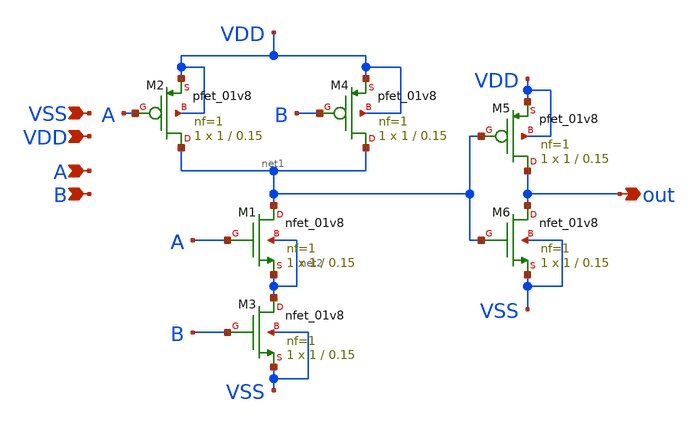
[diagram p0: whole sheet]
** sch_path: and/and2.sch
**.subckt and2 VDD A B VSS out
*.ipin VDD
*.ipin A
*.ipin B
*.ipin VSS
*.opin out
XM1 net1 A net2 net2 sky130_fd_pr__nfet_01v8 L=0.15 W=1 nf=1 ad='int((nf+1)/2) * W/nf * 0.29' as='int((nf+2)/2) * W/nf * 0.29'
+ pd='2*int((nf+1)/2) * (W/nf + 0.29)' ps='2*int((nf+2)/2) * (W/nf + 0.29)' nrd='0.29 / W' nrs='0.29 / W'
+ sa=0 sb=0 sd=0 mult=1 m=1
XM2 net1 A VDD VDD sky130_fd_pr__pfet_01v8 L=0.15 W=1 nf=1 ad='int((nf+1)/2) * W/nf * 0.29' as='int((nf+2)/2) * W/nf * 0.29'
+ pd='2*int((nf+1)/2) * (W/nf + 0.29)' ps='2*int((nf+2)/2) * (W/nf + 0.29)' nrd='0.29 / W' nrs='0.29 / W'
+ sa=0 sb=0 sd=0 mult=1 m=1
XM3 net2 B VSS VSS sky130_fd_pr__nfet_01v8 L=0.15 W=1 nf=1 ad='int((nf+1)/2) * W/nf * 0.29' as='int((nf+2)/2) * W/nf * 0.29'
+ pd='2*int((nf+1)/2) * (W/nf + 0.29)' ps='2*int((nf+2)/2) * (W/nf + 0.29)' nrd='0.29 / W' nrs='0.29 / W'
+ sa=0 sb=0 sd=0 mult=1 m=1
XM4 net1 B VDD VDD sky130_fd_pr__pfet_01v8 L=0.15 W=1 nf=1 ad='int((nf+1)/2) * W/nf * 0.29' as='int((nf+2)/2) * W/nf * 0.29'
+ pd='2*int((nf+1)/2) * (W/nf + 0.29)' ps='2*int((nf+2)/2) * (W/nf + 0.29)' nrd='0.29 / W' nrs='0.29 / W'
+ sa=0 sb=0 sd=0 mult=1 m=1
XM5 out net1 VDD VDD sky130_fd_pr__pfet_01v8 L=0.15 W=1 nf=1 ad='int((nf+1)/2) * W/nf * 0.29' as='int((nf+2)/2) * W/nf * 0.29'
+ pd='2*int((nf+1)/2) * (W/nf + 0.29)' ps='2*int((nf+2)/2) * (W/nf + 0.29)' nrd='0.29 / W' nrs='0.29 / W'
+ sa=0 sb=0 sd=0 mult=1 m=1
XM6 out net1 VSS VSS sky130_fd_pr__nfet_01v8 L=0.15 W=1 nf=1 ad='int((nf+1)/2) * W/nf * 0.29' as='int((nf+2)/2) * W/nf * 0.29'
+ pd='2*int((nf+1)/2) * (W/nf + 0.29)' ps='2*int((nf+2)/2) * (W/nf + 0.29)' nrd='0.29 / W' nrs='0.29 / W'
+ sa=0 sb=0 sd=0 mult=1 m=1
**.ends
.end
